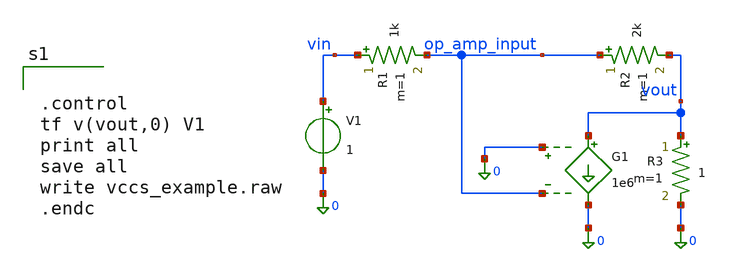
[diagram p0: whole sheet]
** sch_path: mag/vccs_example.sch
**.subckt vccs_example
G1 vout 0 0 op_amp_input 1e6
R1 vin op_amp_input 1k m=1
R2 op_amp_input vout 2k m=1
R3 vout 0 1 m=1
V1 vin 0 1
**** begin user architecture code


.control
tf v(vout,0) V1
print all
save all
write vccs_example.raw
.endc

**** end user architecture code
**.ends
.end
